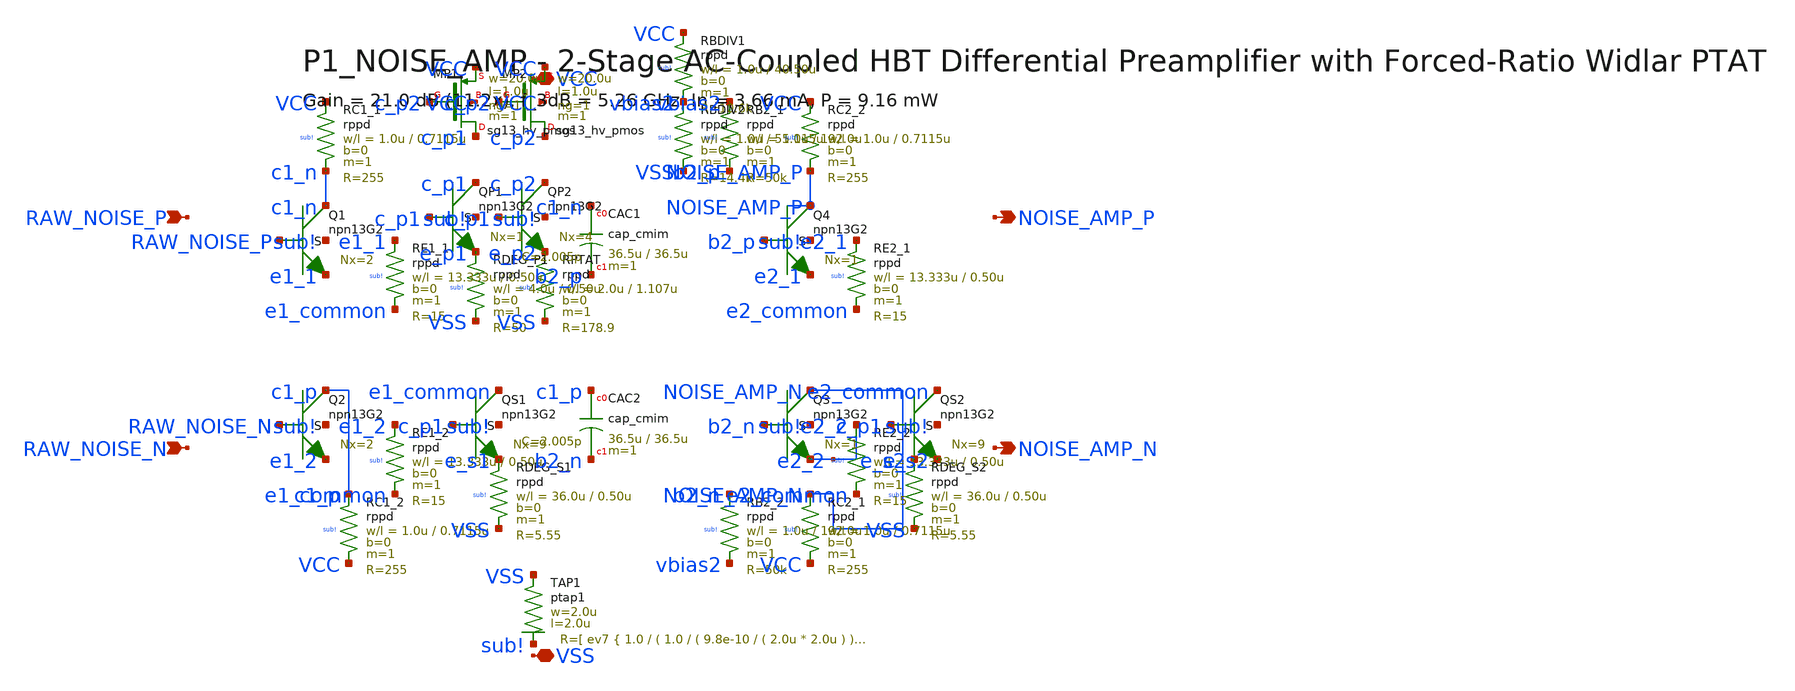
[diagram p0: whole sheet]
** sch_path: designs/p1-pbit/top/source-backed-v2/p1_noise_amp.sch
**.subckt p1_noise_amp NOISE_AMP_P NOISE_AMP_N RAW_NOISE_P RAW_NOISE_N VCC VSS
*.opin NOISE_AMP_P
*.opin NOISE_AMP_N
*.ipin RAW_NOISE_P
*.ipin RAW_NOISE_N
*.iopin VCC
*.iopin VSS
XQ1 c1_n RAW_NOISE_P e1_1 sub! npn13G2 Nx=2 mm_ok=1
XQ2 c1_p RAW_NOISE_N e1_2 sub! npn13G2 Nx=2 mm_ok=1
XRC1_1 VCC c1_n sub! rppd w=1.0u l=0.7115u m=1 b=0 mm_ok=1
XRC1_2 c1_p VCC sub! rppd w=1.0u l=0.7115u m=1 b=0 mm_ok=1
XRE1_1 e1_1 e1_common sub! rppd w=13.333u l=0.50u m=1 b=0 mm_ok=1
XRE1_2 e1_2 e1_common sub! rppd w=13.333u l=0.50u m=1 b=0 mm_ok=1
XMP1 c_p1 c_p2 VCC VCC sg13_hv_pmos w=20.0u l=1.0u ng=1 m=1 mm_ok=1
XMP2 c_p2 c_p2 VCC VCC sg13_hv_pmos w=20.0u l=1.0u ng=1 m=1 mm_ok=1
XQP1 c_p1 c_p1 e_p1 sub! npn13G2 Nx=1 mm_ok=1
XRDEG_P1 e_p1 VSS sub! rppd w=4.0u l=0.50u m=1 b=0 mm_ok=1
XQP2 c_p2 c_p1 e_p2 sub! npn13G2 Nx=4 mm_ok=1
XRPTAT e_p2 VSS sub! rppd w=2.0u l=1.107u m=1 b=0 mm_ok=1
XQS1 e1_common c_p1 e_s1 sub! npn13G2 Nx=9 mm_ok=1
XRDEG_S1 e_s1 VSS sub! rppd w=36.0u l=0.50u m=1 b=0 mm_ok=1
XCAC1 c1_n b2_p cap_cmim w=36.5u l=36.5u m=1 mm_ok=1
XCAC2 c1_p b2_n cap_cmim w=36.5u l=36.5u m=1 mm_ok=1
XRBDIV1 VCC vbias2 sub! rppd w=1.0u l=40.50u m=1 b=0 mm_ok=1
XRBDIV2 vbias2 VSS sub! rppd w=1.0u l=55.115u m=1 b=0 mm_ok=1
XRB2_1 vbias2 b2_p sub! rppd w=1.0u l=192.0u m=1 b=0 mm_ok=1
XRB2_2 b2_n vbias2 sub! rppd w=1.0u l=192.0u m=1 b=0 mm_ok=1
XQ4 NOISE_AMP_P b2_p e2_1 sub! npn13G2 Nx=1 mm_ok=1
XQ3 NOISE_AMP_N b2_n e2_2 sub! npn13G2 Nx=1 mm_ok=1
XRC2_2 VCC NOISE_AMP_P sub! rppd w=1.0u l=0.7115u m=1 b=0 mm_ok=1
XRC2_1 NOISE_AMP_N VCC sub! rppd w=1.0u l=0.7115u m=1 b=0 mm_ok=1
XRE2_1 e2_1 e2_common sub! rppd w=13.333u l=0.50u m=1 b=0 mm_ok=1
XRE2_2 e2_2 e2_common sub! rppd w=13.333u l=0.50u m=1 b=0 mm_ok=1
XQS2 e2_common c_p1 e_s2 sub! npn13G2 Nx=9 mm_ok=1
XRDEG_S2 e_s2 VSS sub! rppd w=36.0u l=0.50u m=1 b=0 mm_ok=1
XTAP1 VSS sub! ptap1 R=81.67 w=2.0u l=2.0u
**.ends
.end
